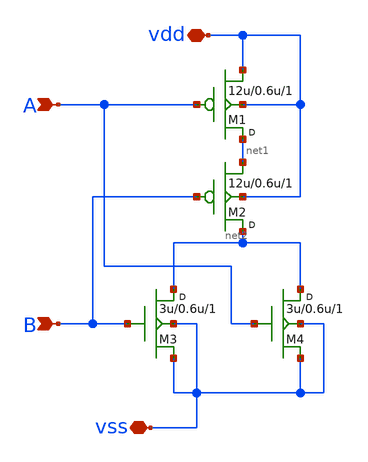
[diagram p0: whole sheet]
** sch_path: lab6/NORx.sch
**.subckt NORx A B vdd vss
*.ipin A
*.ipin B
*.iopin vdd
*.iopin vss
M4 net2 A vss vss nfet w=3u l=0.6u m=1
M1 net1 A vdd vdd pfet w=12u l=0.6u m=1
M2 net2 B net1 vdd pfet w=12u l=0.6u m=1
M3 net2 B vss vss nfet w=3u l=0.6u m=1
**.ends
.end
